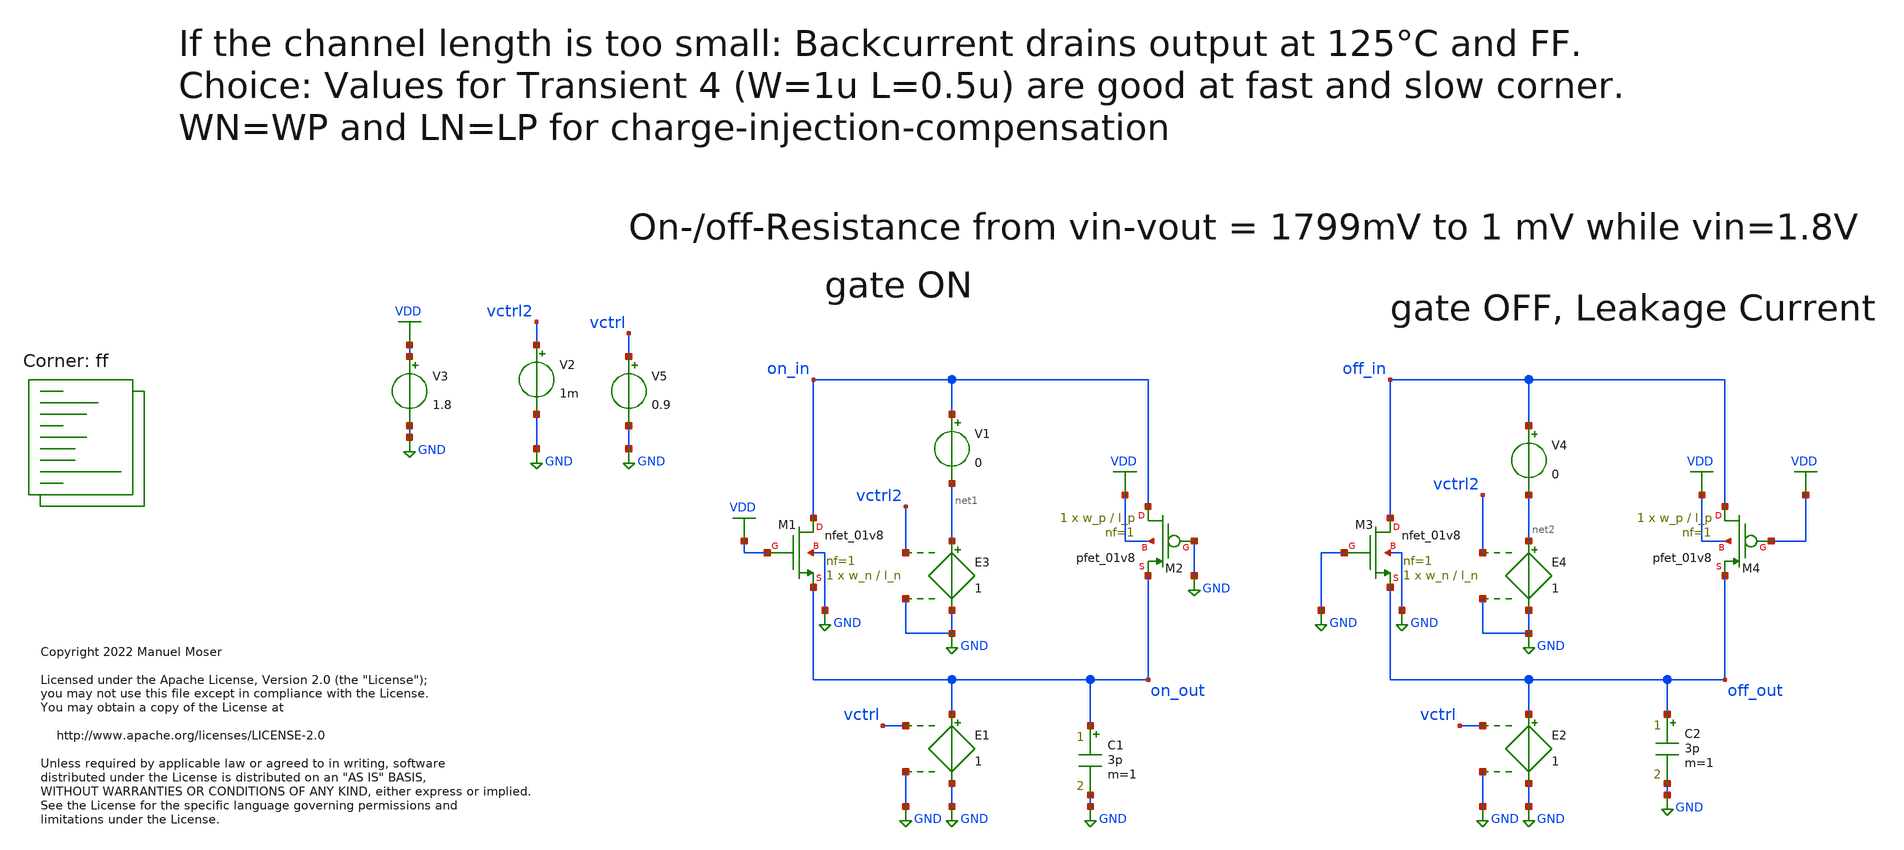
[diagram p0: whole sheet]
** sch_path: xschem/adc_vcm_switch_tb_resistance.sch
* Copyright 2022 Manuel Moser
* Licensed under the Apache License, Version 2.0 (the "License");
**.subckt adc_vcm_switch_tb_resistance
V5 vctrl GND 0.9
XM1 on_in VDD on_out GND sky130_fd_pr__nfet_01v8 L=l_n W=w_n nf=1 ad='int((nf+1)/2) * W/nf * 0.29' as='int((nf+2)/2) * W/nf * 0.29'
+ pd='2*int((nf+1)/2) * (W/nf + 0.29)' ps='2*int((nf+2)/2) * (W/nf + 0.29)' nrd='0.29 / W' nrs='0.29 / W'
+ sa=0 sb=0 sd=0 mult=1 m=1
XM2 on_in GND on_out VDD sky130_fd_pr__pfet_01v8 L=l_p W=w_p nf=1 ad='int((nf+1)/2) * W/nf * 0.29' as='int((nf+2)/2) * W/nf * 0.29'
+ pd='2*int((nf+1)/2) * (W/nf + 0.29)' ps='2*int((nf+2)/2) * (W/nf + 0.29)' nrd='0.29 / W' nrs='0.29 / W'
+ sa=0 sb=0 sd=0 mult=1 m=1
XM3 off_in GND off_out GND sky130_fd_pr__nfet_01v8 L=l_n W=w_n nf=1 ad='int((nf+1)/2) * W/nf * 0.29'
+ as='int((nf+2)/2) * W/nf * 0.29' pd='2*int((nf+1)/2) * (W/nf + 0.29)' ps='2*int((nf+2)/2) * (W/nf + 0.29)'
+ nrd='0.29 / W' nrs='0.29 / W' sa=0 sb=0 sd=0 mult=1 m=1
XM4 off_in VDD off_out VDD sky130_fd_pr__pfet_01v8 L=l_p W=w_p nf=1 ad='int((nf+1)/2) * W/nf * 0.29'
+ as='int((nf+2)/2) * W/nf * 0.29' pd='2*int((nf+1)/2) * (W/nf + 0.29)' ps='2*int((nf+2)/2) * (W/nf + 0.29)'
+ nrd='0.29 / W' nrs='0.29 / W' sa=0 sb=0 sd=0 mult=1 m=1
V2 vctrl2 GND 1m
E1 on_out GND vctrl GND 1
E2 off_out GND vctrl GND 1
C1 on_out GND 3p m=1
C2 off_out GND 3p m=1
E3 net1 GND vctrl2 GND 1
E4 net2 GND vctrl2 GND 1
V4 off_in net2 0
V1 on_in net1 0
V3 VDD GND 1.8
**** begin user architecture code
.lib $::SKYWATER_MODELS/sky130.lib.spice ff


.save all
.temp = 100
*.options method=gear
.OPTIONS savecurrents
*.OPTIONS RELTOL=.1 TRTOL=1 ABSTOL=1e-20 CHGTOL=1.0e-20 DEFAD=1.0e-18
.save @m.x1.xm1.msky130_fd_pr__pfet_01v8[gm]
.save @m.x1.xm1.msky130_fd_pr__pfet_01v8[CGS]
.save @m.x1.xm1.msky130_fd_pr__pfet_01v8[Vth]
.save @m.x1.xm2.msky130_fd_pr__nfet_01v8_lvt[gm]
.save @m.x1.xm2.msky130_fd_pr__nfet_01v8_lvt[CGS]
.save @m.x1.xm2.msky130_fd_pr__nfet_01v8_lvt[Vth]


.param w_p=1
.param l_p = 1
.param w_n=1
.param l_n=1

.dc V5 10m 1790m 10m V2 0m 1800m 1800m

.control
alterparam w_p=0.42
alterparam l_p=0.15
alterparam w_n=0.42
alterparam l_n=0.15
reset
run
write dc-sweep.out v(on_in) v(on_out) v(off_in) v(off_out) I(v1) I(v4)
set appendwrite


alterparam w_p=0.42
alterparam l_p=0.2
alterparam w_n=0.42
alterparam l_n=0.2
reset
run
write dc-sweep.out v(on_in) v(on_out) v(off_in) v(off_out) I(v1) I(v4)
set appendwrite


alterparam w_p=0.42
alterparam l_p=0.5
alterparam w_n=0.42
alterparam l_n=0.5
reset
run
write dc-sweep.out v(on_in) v(on_out) v(off_in) v(off_out) I(v1) I(v4)
set appendwrite

alterparam w_p=1
alterparam l_p=0.5
alterparam w_n=1
alterparam l_n=0.5
reset
run
write dc-sweep.out v(on_in) v(on_out) v(off_in) v(off_out) I(v1) I(v4)
set appendwrite

alterparam w_p=4
alterparam l_p=0.4
alterparam w_n=4
alterparam l_n=0.4
reset
run
write dc-sweep.out v(on_in) v(on_out) v(off_in) v(off_out) I(v1) I(v4)
set appendwrite

*On-Resistance
plot (-(dc1.v(on_in)-dc1.v(on_out))/dc1.I(v1))  (-(dc2.v(on_in)-dc2.v(on_out))/dc2.I(v1)) (-(dc3.v(on_in)-dc3.v(on_out))/dc3.I(v1))
+ (-(dc4.v(on_in)-dc4.v(on_out))/dc4.I(v1)) (-(dc5.v(on_in)-dc5.v(on_out))/dc5.I(v1)) title 'ON-Resistance at VIN=1.8 VIN=0'
*Leakage Current
plot (-dc1.I(v4)) (-dc2.I(v4)) (-dc3.I(v4)) (-dc4.I(v4)) (-dc5.I(v4)) ylimit -100p 100p title 'ON-Resistance at VIN=1.8 VIN=0'
.endc


**** end user architecture code
**.ends
.GLOBAL GND
.GLOBAL VDD
.end
